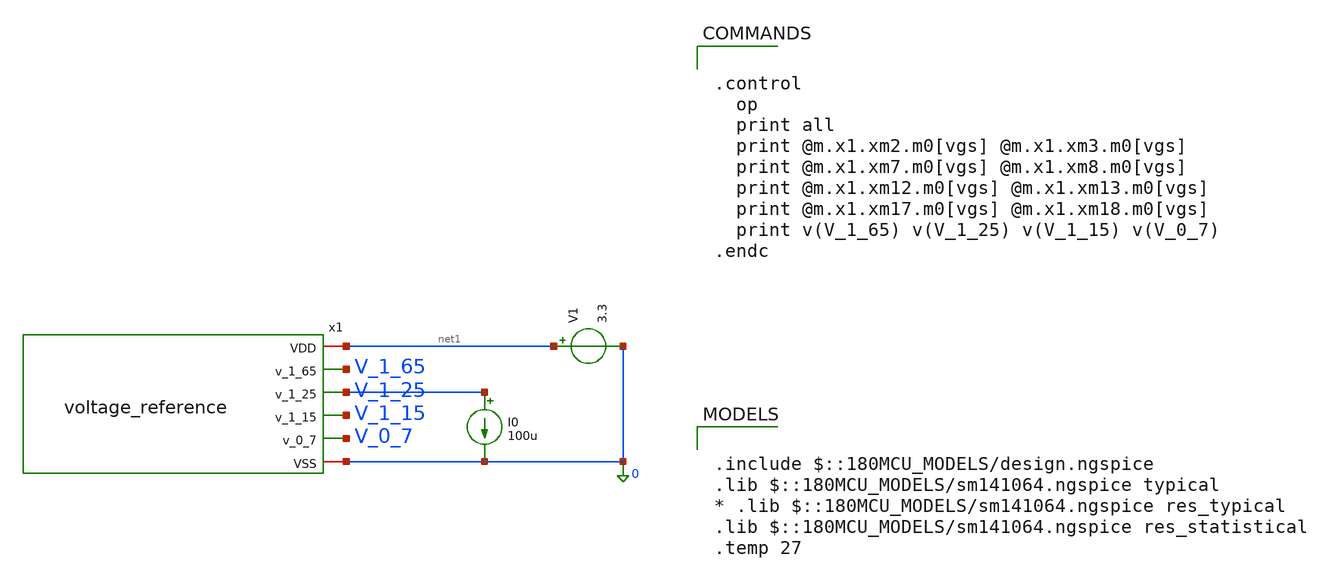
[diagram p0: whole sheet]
** sch_path: schematics/tb_voltage_reference.sch
**.subckt tb_voltage_reference
x1 net1 V_1_65 V_1_25 V_1_15 V_0_7 0 voltage_reference
V1 net1 0 3.3
I0 V_1_25 0 100u
**** begin user architecture code

.include $::180MCU_MODELS/design.ngspice
.lib $::180MCU_MODELS/sm141064.ngspice typical
* .lib $::180MCU_MODELS/sm141064.ngspice res_typical
.lib $::180MCU_MODELS/sm141064.ngspice res_statistical
.temp 27



.control
  op
  print all
  print @m.x1.xm2.m0[vgs] @m.x1.xm3.m0[vgs]
  print @m.x1.xm7.m0[vgs] @m.x1.xm8.m0[vgs]
  print @m.x1.xm12.m0[vgs] @m.x1.xm13.m0[vgs]
  print @m.x1.xm17.m0[vgs] @m.x1.xm18.m0[vgs]
  print v(V_1_65) v(V_1_25) v(V_1_15) v(V_0_7)
.endc


**** end user architecture code
**.ends

* expanding   symbol:  analog-perceptron-gf180mcu/schematics/voltage_reference.sym # of pins=6
** sym_path: schematics/voltage_reference.sym
** sch_path: schematics/voltage_reference.sch
.subckt voltage_reference VDD v_1_65 v_1_25 v_1_15 v_0_7 VSS
*.iopin VDD
*.iopin VSS
*.opin v_1_65
*.opin v_1_15
*.opin v_0_7
*.opin v_1_25
XR1 V_I_1_65 VDD VSS ppolyf_u_1k r_width=3e-6 r_length=165e-6 m=1
XR2 V_I_1_25 V_I_1_65 VSS ppolyf_u_1k r_width=3e-6 r_length=40e-6 m=1
XR3 V_I_1_15 V_I_1_25 VSS ppolyf_u_1k r_width=3e-6 r_length=10e-6 m=1
XR4 V_I_0_7 V_I_1_15 VSS ppolyf_u_1k r_width=3e-6 r_length=45e-6 m=1
XR5 VSS V_I_0_7 VSS ppolyf_u_1k r_width=3e-6 r_length=70e-6 m=1
XM11 net2 V_pbias VDD VDD pfet_03v3 L=1u W=20u nf=1 ad='int((nf+1)/2) * W/nf * 0.18u' as='int((nf+2)/2) * W/nf * 0.18u'
+ pd='2*int((nf+1)/2) * (W/nf + 0.18u)' ps='2*int((nf+2)/2) * (W/nf + 0.18u)' nrd='0.18u / W' nrs='0.18u / W'
+ sa=0 sb=0 sd=0 m=1
XM12 net1 V_I_1_15 net2 VDD pfet_03v3 L=1u W=20u nf=1 ad='int((nf+1)/2) * W/nf * 0.18u' as='int((nf+2)/2) * W/nf * 0.18u'
+ pd='2*int((nf+1)/2) * (W/nf + 0.18u)' ps='2*int((nf+2)/2) * (W/nf + 0.18u)' nrd='0.18u / W' nrs='0.18u / W'
+ sa=0 sb=0 sd=0 m=1
XM13 v_1_15 v_1_15 net2 VDD pfet_03v3 L=1u W=20u nf=1 ad='int((nf+1)/2) * W/nf * 0.18u' as='int((nf+2)/2) * W/nf * 0.18u'
+ pd='2*int((nf+1)/2) * (W/nf + 0.18u)' ps='2*int((nf+2)/2) * (W/nf + 0.18u)' nrd='0.18u / W' nrs='0.18u / W'
+ sa=0 sb=0 sd=0 m=1
XM14 net1 net1 VSS VSS nfet_03v3 L=1u W=10u nf=1 ad='int((nf+1)/2) * W/nf * 0.18u' as='int((nf+2)/2) * W/nf * 0.18u'
+ pd='2*int((nf+1)/2) * (W/nf + 0.18u)' ps='2*int((nf+2)/2) * (W/nf + 0.18u)' nrd='0.18u / W' nrs='0.18u / W'
+ sa=0 sb=0 sd=0 m=1
XM15 v_1_15 net1 VSS VSS nfet_03v3 L=1u W=10u nf=1 ad='int((nf+1)/2) * W/nf * 0.18u' as='int((nf+2)/2) * W/nf * 0.18u'
+ pd='2*int((nf+1)/2) * (W/nf + 0.18u)' ps='2*int((nf+2)/2) * (W/nf + 0.18u)' nrd='0.18u / W' nrs='0.18u / W'
+ sa=0 sb=0 sd=0 m=1
XM16 net4 V_pbias VDD VDD pfet_03v3 L=1u W=20u nf=1 ad='int((nf+1)/2) * W/nf * 0.18u' as='int((nf+2)/2) * W/nf * 0.18u'
+ pd='2*int((nf+1)/2) * (W/nf + 0.18u)' ps='2*int((nf+2)/2) * (W/nf + 0.18u)' nrd='0.18u / W' nrs='0.18u / W'
+ sa=0 sb=0 sd=0 m=1
XM17 net3 V_I_0_7 net4 VDD pfet_03v3 L=1u W=20u nf=1 ad='int((nf+1)/2) * W/nf * 0.18u' as='int((nf+2)/2) * W/nf * 0.18u'
+ pd='2*int((nf+1)/2) * (W/nf + 0.18u)' ps='2*int((nf+2)/2) * (W/nf + 0.18u)' nrd='0.18u / W' nrs='0.18u / W'
+ sa=0 sb=0 sd=0 m=1
XM18 v_0_7 v_0_7 net4 VDD pfet_03v3 L=1u W=20u nf=1 ad='int((nf+1)/2) * W/nf * 0.18u' as='int((nf+2)/2) * W/nf * 0.18u'
+ pd='2*int((nf+1)/2) * (W/nf + 0.18u)' ps='2*int((nf+2)/2) * (W/nf + 0.18u)' nrd='0.18u / W' nrs='0.18u / W'
+ sa=0 sb=0 sd=0 m=1
XM19 net3 net3 VSS VSS nfet_03v3 L=1u W=10u nf=1 ad='int((nf+1)/2) * W/nf * 0.18u' as='int((nf+2)/2) * W/nf * 0.18u'
+ pd='2*int((nf+1)/2) * (W/nf + 0.18u)' ps='2*int((nf+2)/2) * (W/nf + 0.18u)' nrd='0.18u / W' nrs='0.18u / W'
+ sa=0 sb=0 sd=0 m=1
XM20 v_0_7 net3 VSS VSS nfet_03v3 L=1u W=10u nf=1 ad='int((nf+1)/2) * W/nf * 0.18u' as='int((nf+2)/2) * W/nf * 0.18u'
+ pd='2*int((nf+1)/2) * (W/nf + 0.18u)' ps='2*int((nf+2)/2) * (W/nf + 0.18u)' nrd='0.18u / W' nrs='0.18u / W'
+ sa=0 sb=0 sd=0 m=1
XM21 VDD net10 v_1_25 VSS nfet_03v3 L=1u W=100u nf=1 ad='int((nf+1)/2) * W/nf * 0.18u' as='int((nf+2)/2) * W/nf * 0.18u'
+ pd='2*int((nf+1)/2) * (W/nf + 0.18u)' ps='2*int((nf+2)/2) * (W/nf + 0.18u)' nrd='0.18u / W' nrs='0.18u / W'
+ sa=0 sb=0 sd=0 m=1
XR6 VSS v_1_25 VSS ppolyf_u_1k r_width=3e-6 r_length=30e-6 m=1
XM22 V_pbias V_pbias VDD VDD pfet_03v3 L=1u W=10u nf=1 ad='int((nf+1)/2) * W/nf * 0.18u' as='int((nf+2)/2) * W/nf * 0.18u'
+ pd='2*int((nf+1)/2) * (W/nf + 0.18u)' ps='2*int((nf+2)/2) * (W/nf + 0.18u)' nrd='0.18u / W' nrs='0.18u / W'
+ sa=0 sb=0 sd=0 m=1
XR7 VSS V_pbias VSS ppolyf_u_1k r_width=3e-6 r_length=150e-6 m=1
XM1 net6 V_I_1_65 net5 VSS nfet_03v3 L=2u W=10u nf=1 ad='int((nf+1)/2) * W/nf * 0.18u' as='int((nf+2)/2) * W/nf * 0.18u'
+ pd='2*int((nf+1)/2) * (W/nf + 0.18u)' ps='2*int((nf+2)/2) * (W/nf + 0.18u)' nrd='0.18u / W' nrs='0.18u / W'
+ sa=0 sb=0 sd=0 m=1
XM2 net7 v_1_65 net5 VSS nfet_03v3 L=2u W=10u nf=1 ad='int((nf+1)/2) * W/nf * 0.18u' as='int((nf+2)/2) * W/nf * 0.18u'
+ pd='2*int((nf+1)/2) * (W/nf + 0.18u)' ps='2*int((nf+2)/2) * (W/nf + 0.18u)' nrd='0.18u / W' nrs='0.18u / W'
+ sa=0 sb=0 sd=0 m=1
XM3 net5 V_nbias VSS VSS nfet_03v3 L=2u W=10u nf=1 ad='int((nf+1)/2) * W/nf * 0.18u' as='int((nf+2)/2) * W/nf * 0.18u'
+ pd='2*int((nf+1)/2) * (W/nf + 0.18u)' ps='2*int((nf+2)/2) * (W/nf + 0.18u)' nrd='0.18u / W' nrs='0.18u / W'
+ sa=0 sb=0 sd=0 m=1
XM4 net6 net6 VDD VDD pfet_03v3 L=2u W=20u nf=1 ad='int((nf+1)/2) * W/nf * 0.18u' as='int((nf+2)/2) * W/nf * 0.18u'
+ pd='2*int((nf+1)/2) * (W/nf + 0.18u)' ps='2*int((nf+2)/2) * (W/nf + 0.18u)' nrd='0.18u / W' nrs='0.18u / W'
+ sa=0 sb=0 sd=0 m=1
XM5 net7 net6 VDD VDD pfet_03v3 L=2u W=20u nf=1 ad='int((nf+1)/2) * W/nf * 0.18u' as='int((nf+2)/2) * W/nf * 0.18u'
+ pd='2*int((nf+1)/2) * (W/nf + 0.18u)' ps='2*int((nf+2)/2) * (W/nf + 0.18u)' nrd='0.18u / W' nrs='0.18u / W'
+ sa=0 sb=0 sd=0 m=1
XM23 V_nbias V_nbias VSS VSS nfet_03v3 L=1u W=10u nf=1 ad='int((nf+1)/2) * W/nf * 0.18u' as='int((nf+2)/2) * W/nf * 0.18u'
+ pd='2*int((nf+1)/2) * (W/nf + 0.18u)' ps='2*int((nf+2)/2) * (W/nf + 0.18u)' nrd='0.18u / W' nrs='0.18u / W'
+ sa=0 sb=0 sd=0 m=1
XR8 V_nbias VDD VSS ppolyf_u_1k r_width=3e-6 r_length=150e-6 m=1
XM6 net9 V_I_1_25 net8 VSS nfet_03v3 L=2u W=10u nf=1 ad='int((nf+1)/2) * W/nf * 0.18u' as='int((nf+2)/2) * W/nf * 0.18u'
+ pd='2*int((nf+1)/2) * (W/nf + 0.18u)' ps='2*int((nf+2)/2) * (W/nf + 0.18u)' nrd='0.18u / W' nrs='0.18u / W'
+ sa=0 sb=0 sd=0 m=1
XM7 net10 v_1_25 net8 VSS nfet_03v3 L=2u W=10u nf=1 ad='int((nf+1)/2) * W/nf * 0.18u' as='int((nf+2)/2) * W/nf * 0.18u'
+ pd='2*int((nf+1)/2) * (W/nf + 0.18u)' ps='2*int((nf+2)/2) * (W/nf + 0.18u)' nrd='0.18u / W' nrs='0.18u / W'
+ sa=0 sb=0 sd=0 m=1
XM8 net8 V_nbias VSS VSS nfet_03v3 L=2u W=10u nf=1 ad='int((nf+1)/2) * W/nf * 0.18u' as='int((nf+2)/2) * W/nf * 0.18u'
+ pd='2*int((nf+1)/2) * (W/nf + 0.18u)' ps='2*int((nf+2)/2) * (W/nf + 0.18u)' nrd='0.18u / W' nrs='0.18u / W'
+ sa=0 sb=0 sd=0 m=1
XM9 net9 net9 VDD VDD pfet_03v3 L=2u W=20u nf=1 ad='int((nf+1)/2) * W/nf * 0.18u' as='int((nf+2)/2) * W/nf * 0.18u'
+ pd='2*int((nf+1)/2) * (W/nf + 0.18u)' ps='2*int((nf+2)/2) * (W/nf + 0.18u)' nrd='0.18u / W' nrs='0.18u / W'
+ sa=0 sb=0 sd=0 m=1
XM10 net10 net9 VDD VDD pfet_03v3 L=2u W=20u nf=1 ad='int((nf+1)/2) * W/nf * 0.18u' as='int((nf+2)/2) * W/nf * 0.18u'
+ pd='2*int((nf+1)/2) * (W/nf + 0.18u)' ps='2*int((nf+2)/2) * (W/nf + 0.18u)' nrd='0.18u / W' nrs='0.18u / W'
+ sa=0 sb=0 sd=0 m=1
XM24 VDD net7 v_1_65 VSS nfet_03v3 L=1u W=100u nf=1 ad='int((nf+1)/2) * W/nf * 0.18u' as='int((nf+2)/2) * W/nf * 0.18u'
+ pd='2*int((nf+1)/2) * (W/nf + 0.18u)' ps='2*int((nf+2)/2) * (W/nf + 0.18u)' nrd='0.18u / W' nrs='0.18u / W'
+ sa=0 sb=0 sd=0 m=1
XR9 VSS v_1_65 VSS ppolyf_u_1k r_width=3e-6 r_length=30e-6 m=1
.ends

.end
